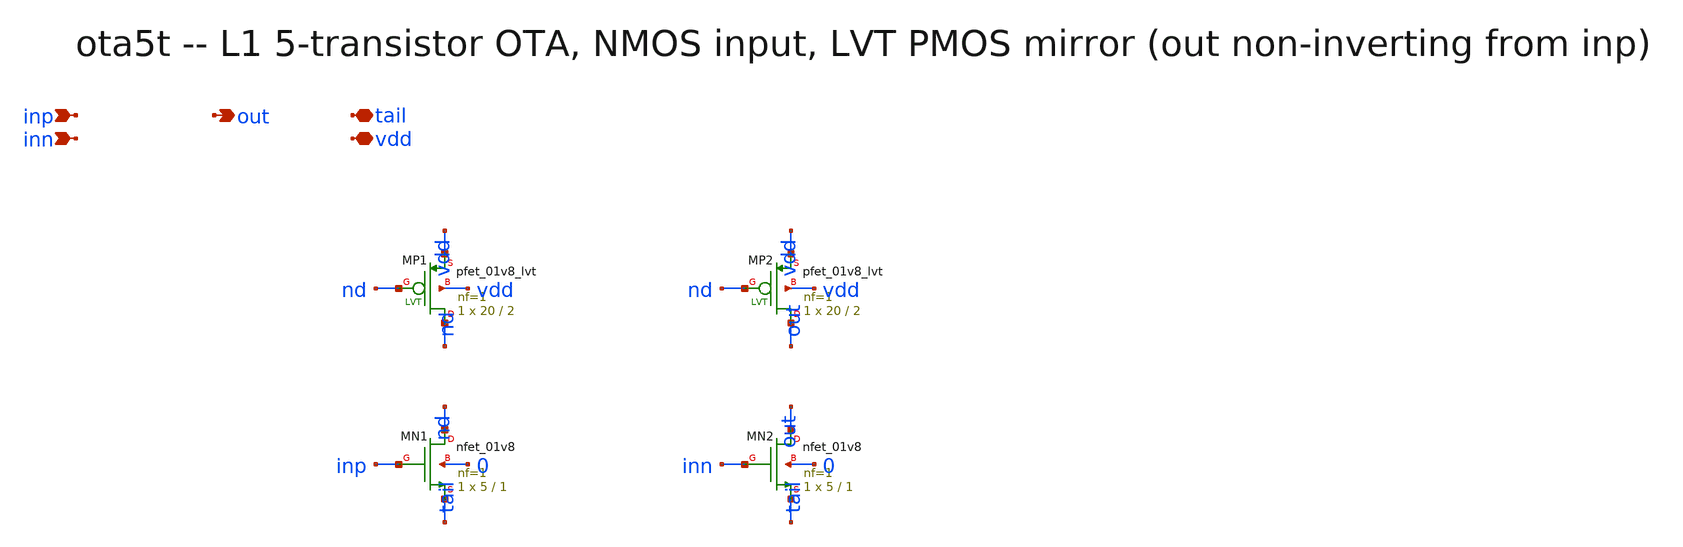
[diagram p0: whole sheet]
** sch_path: xschem/onetops/ota5t.sch
**.subckt ota5t inp inn out tail vdd
*.ipin inp
*.ipin inn
*.opin out
*.iopin tail
*.iopin vdd
XMP1 nd nd vdd vdd sky130_fd_pr__pfet_01v8_lvt L=2 W=20 nf=1 ad='int((1 + 1)/2) * 20 / 1 * 0.29' as='int((1 + 2)/2) * 20 / 1 * 0.29'
+ pd='2*int((1 + 1)/2) * (20 / 1 + 0.29)' ps='2*int((1 + 2)/2) * (20 / 1 + 0.29)' nrd='0.29 / 20 ' nrs='0.29 / 20 '
+ sa=0 sb=0 sd=0 mult=1 m=1
XMP2 out nd vdd vdd sky130_fd_pr__pfet_01v8_lvt L=2 W=20 nf=1 ad='int((1 + 1)/2) * 20 / 1 * 0.29' as='int((1 + 2)/2) * 20 / 1 * 0.29'
+ pd='2*int((1 + 1)/2) * (20 / 1 + 0.29)' ps='2*int((1 + 2)/2) * (20 / 1 + 0.29)' nrd='0.29 / 20 ' nrs='0.29 / 20 '
+ sa=0 sb=0 sd=0 mult=1 m=1
XMN1 nd inp tail 0 sky130_fd_pr__nfet_01v8 L=1 W=5 nf=1 ad='int((1 + 1)/2) * 5 / 1 * 0.29' as='int((1 + 2)/2) * 5 / 1 * 0.29'
+ pd='2*int((1 + 1)/2) * (5 / 1 + 0.29)' ps='2*int((1 + 2)/2) * (5 / 1 + 0.29)' nrd='0.29 / 5 ' nrs='0.29 / 5 '
+ sa=0 sb=0 sd=0 mult=1 m=1
XMN2 out inn tail 0 sky130_fd_pr__nfet_01v8 L=1 W=5 nf=1 ad='int((1 + 1)/2) * 5 / 1 * 0.29' as='int((1 + 2)/2) * 5 / 1 * 0.29'
+ pd='2*int((1 + 1)/2) * (5 / 1 + 0.29)' ps='2*int((1 + 2)/2) * (5 / 1 + 0.29)' nrd='0.29 / 5 ' nrs='0.29 / 5 '
+ sa=0 sb=0 sd=0 mult=1 m=1
**.ends
.end
